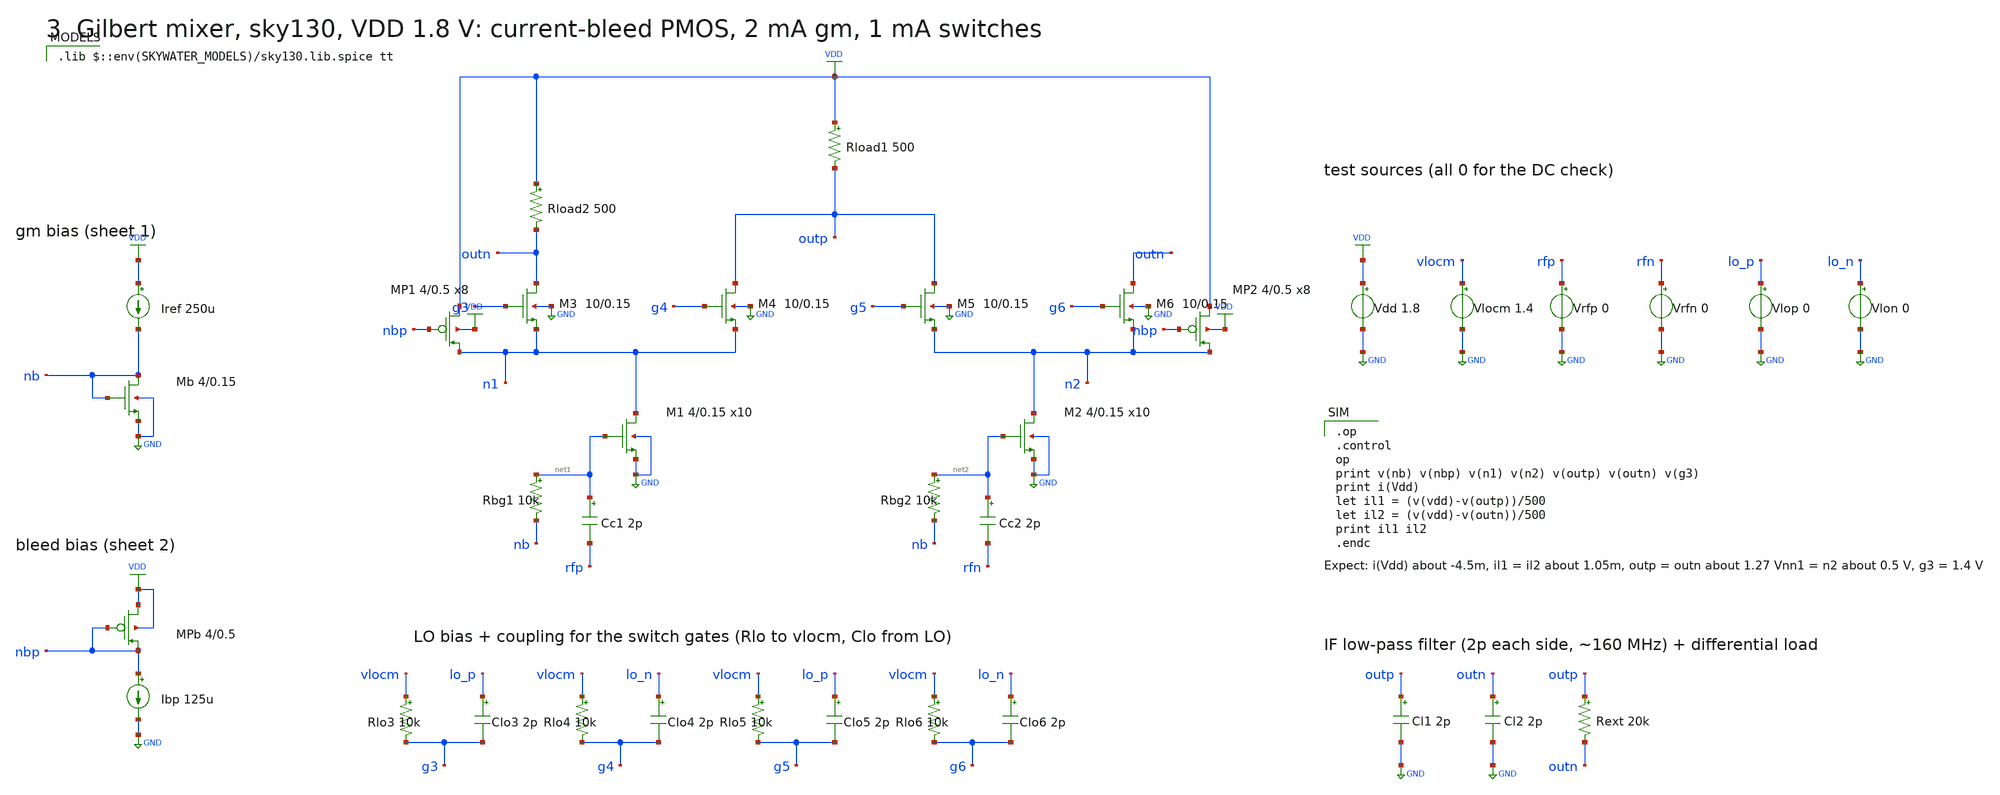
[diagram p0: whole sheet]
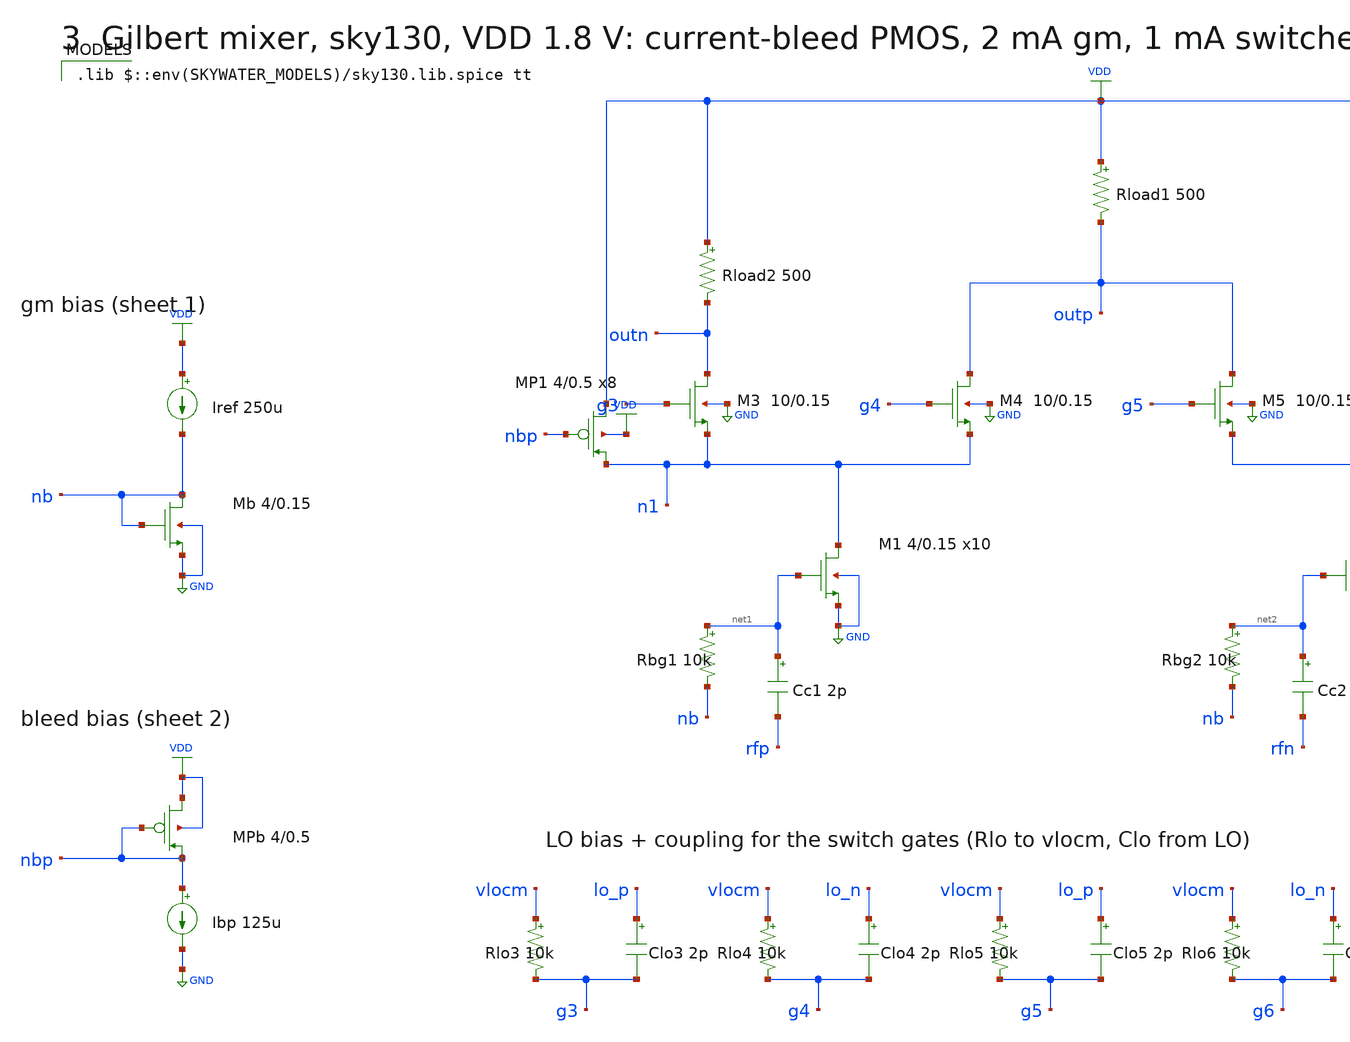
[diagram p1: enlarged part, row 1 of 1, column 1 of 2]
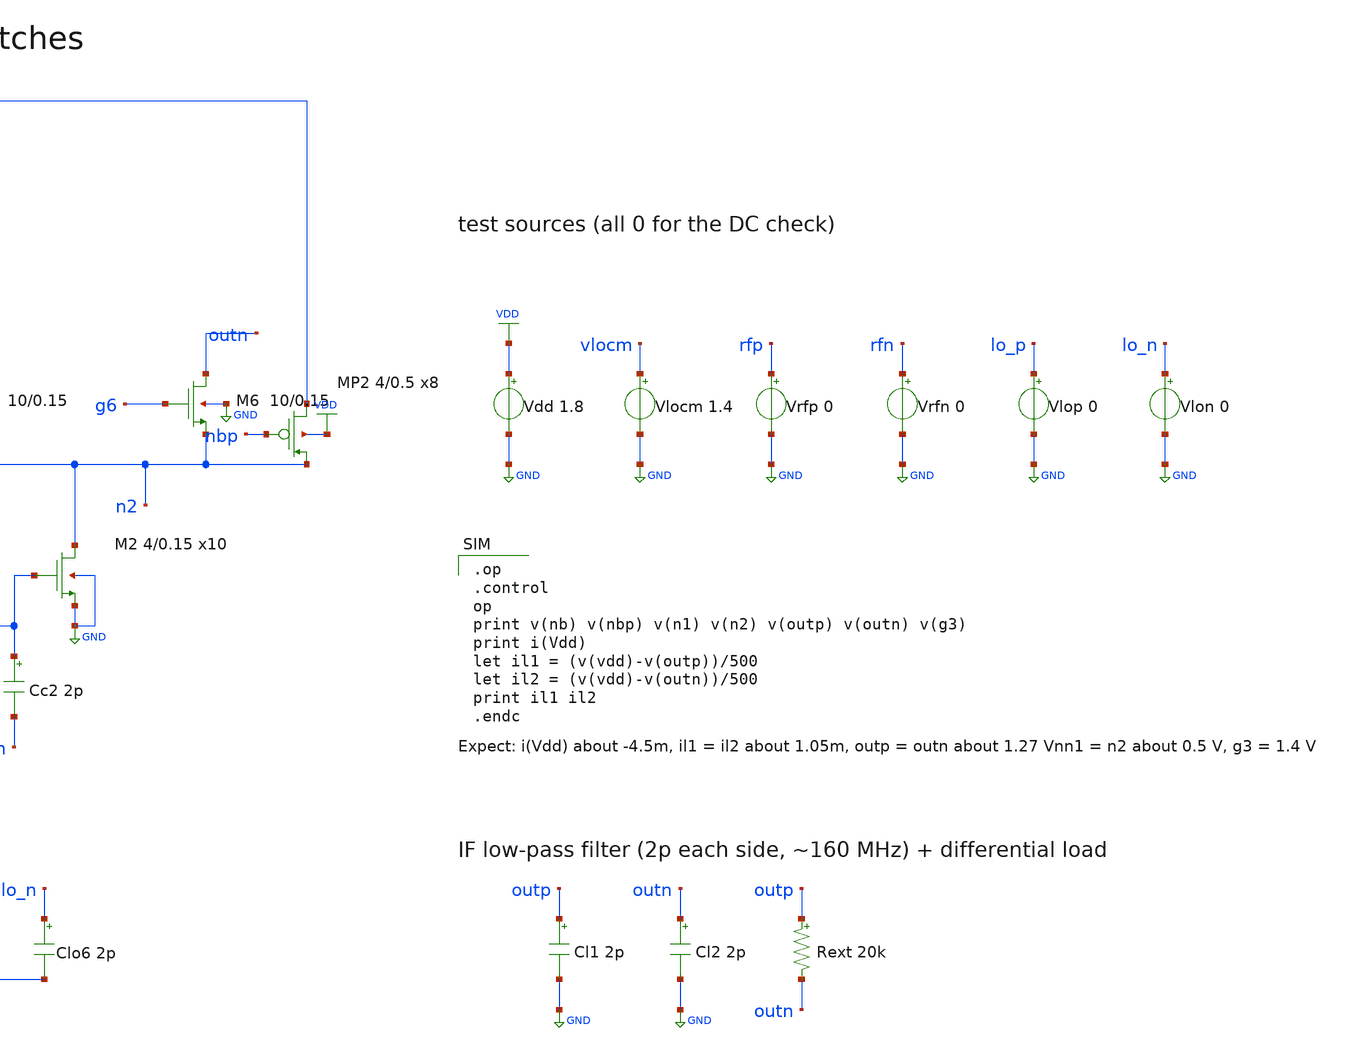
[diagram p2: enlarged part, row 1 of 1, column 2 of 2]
** sch_path: 09-sky130-gilbert-mixer-rfic/schematics/3_gilbert_mixer1.sch
**.subckt 3_gilbert_mixer1
XM3 outn g3 n1 GND sky130_fd_pr__nfet_01v8 L=0.15 W=10 nf=1 ad='int((nf+1)/2) * W/nf * 0.29' as='int((nf+2)/2) * W/nf * 0.29'
+ pd='2*int((nf+1)/2) * (W/nf + 0.29)' ps='2*int((nf+2)/2) * (W/nf + 0.29)' nrd='0.29 / W' nrs='0.29 / W'
+ sa=0 sb=0 sd=0 mult=1 m=1
XM4 outp g4 n1 GND sky130_fd_pr__nfet_01v8 L=0.15 W=10 nf=1 ad='int((nf+1)/2) * W/nf * 0.29' as='int((nf+2)/2) * W/nf * 0.29'
+ pd='2*int((nf+1)/2) * (W/nf + 0.29)' ps='2*int((nf+2)/2) * (W/nf + 0.29)' nrd='0.29 / W' nrs='0.29 / W'
+ sa=0 sb=0 sd=0 mult=1 m=1
XM5 outp g5 n2 GND sky130_fd_pr__nfet_01v8 L=0.15 W=10 nf=1 ad='int((nf+1)/2) * W/nf * 0.29' as='int((nf+2)/2) * W/nf * 0.29'
+ pd='2*int((nf+1)/2) * (W/nf + 0.29)' ps='2*int((nf+2)/2) * (W/nf + 0.29)' nrd='0.29 / W' nrs='0.29 / W'
+ sa=0 sb=0 sd=0 mult=1 m=1
XM6 outn g6 n2 GND sky130_fd_pr__nfet_01v8 L=0.15 W=10 nf=1 ad='int((nf+1)/2) * W/nf * 0.29' as='int((nf+2)/2) * W/nf * 0.29'
+ pd='2*int((nf+1)/2) * (W/nf + 0.29)' ps='2*int((nf+2)/2) * (W/nf + 0.29)' nrd='0.29 / W' nrs='0.29 / W'
+ sa=0 sb=0 sd=0 mult=1 m=1
Rload2 VDD outn 500 m=1
Rload1 VDD outp 500 m=1
XMP1 VDD nbp n1 VDD sky130_fd_pr__pfet_01v8 L=0.5 W=4 nf=1 ad='int((nf+1)/2) * W/nf * 0.29' as='int((nf+2)/2) * W/nf * 0.29'
+ pd='2*int((nf+1)/2) * (W/nf + 0.29)' ps='2*int((nf+2)/2) * (W/nf + 0.29)' nrd='0.29 / W' nrs='0.29 / W'
+ sa=0 sb=0 sd=0 mult=8 m=8
XMP2 VDD nbp n2 VDD sky130_fd_pr__pfet_01v8 L=0.5 W=4 nf=1 ad='int((nf+1)/2) * W/nf * 0.29' as='int((nf+2)/2) * W/nf * 0.29'
+ pd='2*int((nf+1)/2) * (W/nf + 0.29)' ps='2*int((nf+2)/2) * (W/nf + 0.29)' nrd='0.29 / W' nrs='0.29 / W'
+ sa=0 sb=0 sd=0 mult=8 m=8
XM1 n1 net1 GND GND sky130_fd_pr__nfet_01v8 L=0.15 W=4 nf=1 ad='int((nf+1)/2) * W/nf * 0.29' as='int((nf+2)/2) * W/nf * 0.29'
+ pd='2*int((nf+1)/2) * (W/nf + 0.29)' ps='2*int((nf+2)/2) * (W/nf + 0.29)' nrd='0.29 / W' nrs='0.29 / W'
+ sa=0 sb=0 sd=0 mult=10 m=10
Rbg1 net1 nb 10k m=1
Cc1 net1 rfp 2p m=1
XM2 n2 net2 GND GND sky130_fd_pr__nfet_01v8 L=0.15 W=4 nf=1 ad='int((nf+1)/2) * W/nf * 0.29' as='int((nf+2)/2) * W/nf * 0.29'
+ pd='2*int((nf+1)/2) * (W/nf + 0.29)' ps='2*int((nf+2)/2) * (W/nf + 0.29)' nrd='0.29 / W' nrs='0.29 / W'
+ sa=0 sb=0 sd=0 mult=10 m=10
Rbg2 net2 nb 10k m=1
Cc2 net2 rfn 2p m=1
Rlo3 vlocm g3 10k m=1
Clo3 lo_p g3 2p m=1
Rlo4 vlocm g4 10k m=1
Clo4 lo_n g4 2p m=1
Rlo5 vlocm g5 10k m=1
Clo5 lo_p g5 2p m=1
Rlo6 vlocm g6 10k m=1
Clo6 lo_n g6 2p m=1
Iref VDD nb 250u
XMb nb nb GND GND sky130_fd_pr__nfet_01v8 L=0.15 W=4 nf=1 ad='int((nf+1)/2) * W/nf * 0.29' as='int((nf+2)/2) * W/nf * 0.29'
+ pd='2*int((nf+1)/2) * (W/nf + 0.29)' ps='2*int((nf+2)/2) * (W/nf + 0.29)' nrd='0.29 / W' nrs='0.29 / W'
+ sa=0 sb=0 sd=0 mult=1 m=1
XMPb VDD nbp nbp VDD sky130_fd_pr__pfet_01v8 L=0.5 W=4 nf=1 ad='int((nf+1)/2) * W/nf * 0.29' as='int((nf+2)/2) * W/nf * 0.29'
+ pd='2*int((nf+1)/2) * (W/nf + 0.29)' ps='2*int((nf+2)/2) * (W/nf + 0.29)' nrd='0.29 / W' nrs='0.29 / W'
+ sa=0 sb=0 sd=0 mult=1 m=1
Ibp nbp GND 125u
Vdd VDD GND 1.8
Vlocm vlocm GND 1.4
Vrfp rfp GND 0
Vrfn rfn GND 0
Vlop lo_p GND 0
Vlon lo_n GND 0
Cl1 outp GND 2p m=1
Cl2 outn GND 2p m=1
Rext outp outn 20k m=1
**** begin user architecture code
 .lib $::env(SKYWATER_MODELS)/sky130.lib.spice tt

.op
.control
op
print v(nb) v(nbp) v(n1) v(n2) v(outp) v(outn) v(g3)
print i(Vdd)
let il1 = (v(vdd)-v(outp))/500
let il2 = (v(vdd)-v(outn))/500
print il1 il2
.endc

**** end user architecture code
**.ends
.GLOBAL VDD
.GLOBAL GND
.end
